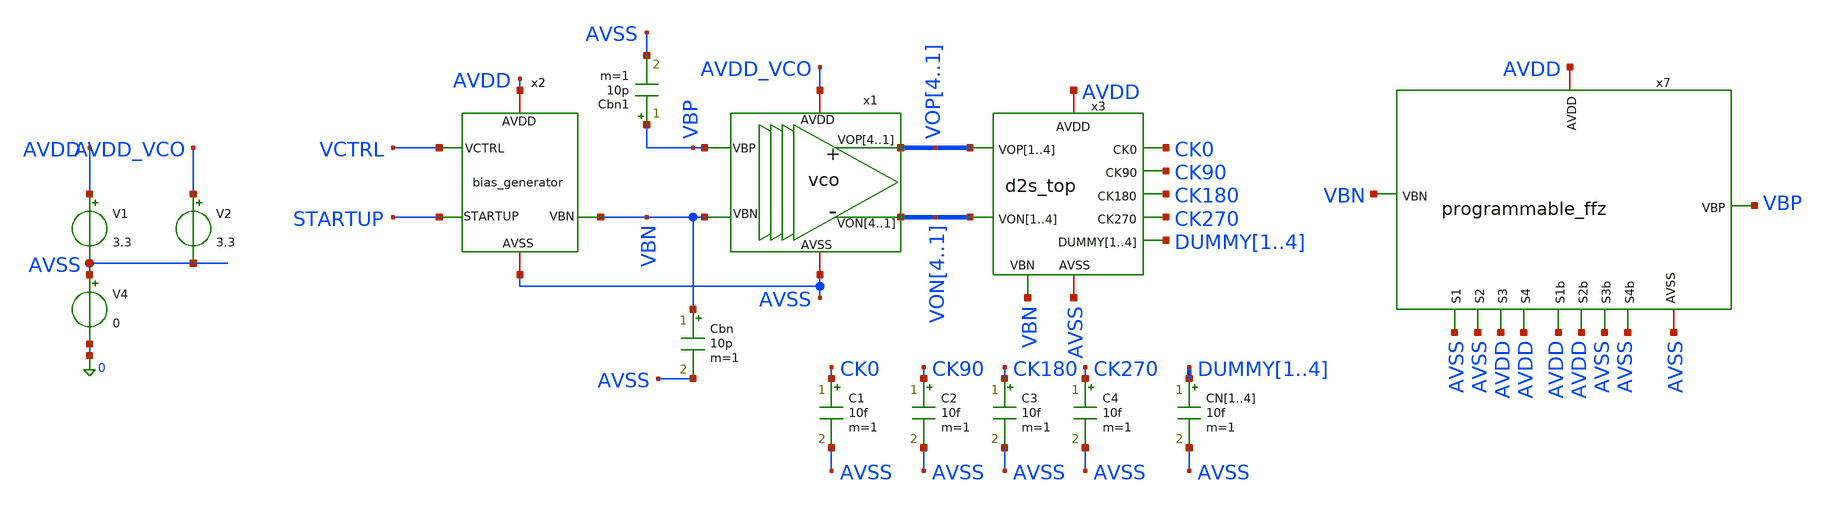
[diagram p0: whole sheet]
** sch_path: designs/libs/tb_analog/tb_quadrature_vco/tb_quadrature_vco.sch
**.subckt tb_quadrature_vco
x1 VOP4 VOP3 VOP2 VOP1 VON4 VON3 VON2 VON1 AVDD_VCO AVSS VBP VBN vco
V1 AVDD AVSS 3.3
V4 AVSS 0 0
CN1 DUMMY1 AVSS 10f m=1
CN2 DUMMY2 AVSS 10f m=1
CN3 DUMMY3 AVSS 10f m=1
CN4 DUMMY4 AVSS 10f m=1
x2 VCTRL AVDD STARTUP AVSS VBN bias_generator
Cbn VBN AVSS 10p m=1
V2 AVDD_VCO AVSS 3.3
Cbn1 VBP AVSS 10p m=1
x7 VBP AVSS AVDD VBN AVDD AVSS AVDD AVSS AVSS AVDD AVSS AVDD programmable_ffz
x3 VOP4 VOP3 VOP2 VOP1 VON4 VON3 VON2 VON1 VBN DUMMY1 DUMMY2 DUMMY3 DUMMY4 CK0 CK90 CK180 CK270 AVDD
+ AVSS d2s_top
C1 CK0 AVSS 10f m=1
C2 CK90 AVSS 10f m=1
C3 CK180 AVSS 10f m=1
C4 CK270 AVSS 10f m=1
**** begin user architecture code


.param Vin=0 Vcm=2.5
.ic v(vop1)=3.3 v(von1)=0 v(startup)=0 v(vbp)=0
.param t1=1u t2=2u t3=3u t4=4u t5=5u t6=6u t7=10u t8=50u t9=500u tr=10n

.param d0=0 d1=0.35 d2=0.825 d3=1.2375 d4=1.65 d5=2.0625 d6=2.475 d7=2.6 d8=2.75

*vs startup 0 pulse(0 1 100n 10n 10n 100n 100m)
*vctrl vctrl 0 pwl(0 d0
*+t1 d0 't1+tr' d1
*+t2 d1 't2+tr' d2
*+t3 d2 't3+tr' d3
*+t4 d3 't4+tr' d4
*+t5 d4 't5+tr' d5
*+t6 d5 't6+tr' d6
*+t7 d6 't7+tr' d7
*+t8 d7 't8+tr' d8
*+t9 d8 't9+tr' d0 R 0)

vctrl vctrl 0 d8

.control
set wr_singlescale
set wr_vecnames

save v(CK0) v(CK90) v(CK180) v(CK270) v(vctrl) v(vbp) v(vbn) v(dummy1) v(dummy2) v(dummy3) v(dummy4)
+ v(VOP1) v(VOP2) v(VOP3) v(VOP4) v(VON1) v(VON2) v(VON3) v(VON4)

OP
show all

*tran 1n 1.5m
tran 10n 500u
*tran 10p 50n



*let sum = v(VOP1) + v(VON1)
*let diff = v(VOP1) - v(VON1)
*let gain = deriv(diff)
*let vcm = AVG(sum/2)


*meas tran vmax MAX v(VOP1) FROM=10n TO=20n
*meas tran vmin MIN v(VOP1) FROM=10n TO=20n
*let vswing = vmax-vmin

meas tran I_tail_avg1 AVG i(v.x1.x1.vmeas) FROM=1.01u TO=2u
meas tran I_tail_avg2 AVG i(v.x1.x1.vmeas) FROM=2.01u TO=3u
meas tran I_tail_avg3 AVG i(v.x1.x1.vmeas) FROM=3.01u TO=4u
meas tran I_tail_avg4 AVG i(v.x1.x1.vmeas) FROM=4.01u TO=5u
meas tran I_tail_avg5 AVG i(v.x1.x1.vmeas) FROM=5.01u TO=6u
meas tran I_tail_avg6 AVG i(v.x1.x1.vmeas) FROM=6.01u TO=10u
meas tran I_tail_avg7 AVG i(v.x1.x1.vmeas) FROM=10.01u TO=50u
meas tran I_tail_avg8 AVG i(v.x1.x1.vmeas) FROM=50.01u TO=500u

*meas tran I_d2s1 AVG i(v.x3.x1.vmeas) FROM=1.01u TO=2u
*meas tran I_d2s2 AVG i(v.x3.x1.vmeas) FROM=2.01u TO=3u
*meas tran I_d2s3 AVG i(v.x3.x1.vmeas) FROM=3.01u TO=4u
*meas tran I_d2s4 AVG i(v.x3.x1.vmeas) FROM=4.01u TO=5u
*meas tran I_d2s5 AVG i(v.x3.x1.vmeas) FROM=5.01u TO=6u
*meas tran I_d2s6 AVG i(v.x3.x1.vmeas) FROM=6.01u TO=10u
*meas tran I_d2s7 AVG i(v.x3.x1.vmeas) FROM=10.01u TO=50u
*meas tran I_d2s8 AVG i(v.x3.x1.vmeas) FROM=50.01u TO=500u

*meas tran I_VCO1 AVG i(V2) FROM=1.01u TO=2u
*meas tran I_VCO2 AVG i(V2) FROM=2.01u TO=3u
*meas tran I_VCO3 AVG i(V2) FROM=3.01u TO=4u
*meas tran I_VCO4 AVG i(V2) FROM=4.01u TO=5u
*meas tran I_VCO5 AVG i(V2) FROM=5.01u TO=6u
*meas tran I_VCO6 AVG i(V2) FROM=6.01u TO=10u
*meas tran I_VCO7 AVG i(V2) FROM=10.01u TO=100u
*meas tran I_VCO8 AVG i(V2) FROM=100.01u TO=1m

remzerovec
*linearize v(CK0) v(CK90) v(CK180) v(CK270)
write tb_quadrature_vco.raw
destroy all
exit
*wrdata
*+ /foss/designs/synchronos-chipathon-2026/designs/libs/scripts/sim_data/tb_quadrature_vco_free_running_test.txt tran.all
.endc



.include $::180MCU_MODELS/design.ngspice
.lib $::180MCU_MODELS/sm141064.ngspice typical
*.lib $::180MCU_MODELS/sm141064.ngspice SS
*.lib $::180MCU_MODELS/sm141064.ngspice FF
*.lib $::180MCU_MODELS/sm141064.ngspice SF
*.lib $::180MCU_MODELS/sm141064.ngspice FS

**** end user architecture code
**.ends

* expanding   symbol:  libs/core_analog/vco/vco.sym # of pins=6
** sym_path: designs/libs/core_analog/vco/vco.sym
** sch_path: designs/libs/core_analog/vco/vco.sch
.subckt vco VOP4 VOP3 VOP2 VOP1 VON4 VON3 VON2 VON1 AVDD AVSS VBP VBN
*.opin VOP1,VOP2,VOP3,VOP4
*.opin VON1,VON2,VON3,VON4
*.ipin VBP
*.ipin VBN
*.iopin AVDD
*.iopin AVSS
x1 VOP1 AVDD VOP4 VON4 VON1 AVSS VBP VBN delay_stage
x2 VOP2 AVDD VON1 VOP1 VON2 AVSS VBP VBN delay_stage
x3 VOP3 AVDD VON2 VOP2 VON3 AVSS VBP VBN delay_stage
x4 VOP4 AVDD VON3 VOP3 VON4 AVSS VBP VBN delay_stage
.ends


* expanding   symbol:  libs/core_analog/bias_generator/bias_generator.sym # of pins=5
** sym_path: designs/libs/core_analog/bias_generator/bias_generator.sym
** sch_path: designs/libs/core_analog/bias_generator/bias_generator.sch
.subckt bias_generator VCTRL AVDD STARTUP AVSS VBN
*.ipin VCTRL
*.ipin STARTUP
*.iopin AVDD
*.iopin AVSS
*.opin VBN
x1 VBN AVDD net2 VCTRL AVSS net1 ota_5t
XM1 net1 net1 AVDD AVDD pfet_03v3 L=0.5u W=16.8u nf=1 ad='int((nf+1)/2) * W/nf * 0.18u' as='int((nf+2)/2) * W/nf * 0.18u'
+ pd='2*int((nf+1)/2) * (W/nf + 0.18u)' ps='2*int((nf+2)/2) * (W/nf + 0.18u)' nrd='0.18u / W' nrs='0.18u / W'
+ sa=0 sb=0 sd=0 m=16
XM8 net2 AVDD net4 AVSS nfet_03v3 L=0.5u W=2.08u nf=1 ad='int((nf+1)/2) * W/nf * 0.18u' as='int((nf+2)/2) * W/nf * 0.18u'
+ pd='2*int((nf+1)/2) * (W/nf + 0.18u)' ps='2*int((nf+2)/2) * (W/nf + 0.18u)' nrd='0.18u / W' nrs='0.18u / W'
+ sa=0 sb=0 sd=0 m=8
XM11 net1 AVDD net3 AVSS nfet_03v3 L=0.5u W=2.08u nf=1 ad='int((nf+1)/2) * W/nf * 0.18u' as='int((nf+2)/2) * W/nf * 0.18u'
+ pd='2*int((nf+1)/2) * (W/nf + 0.18u)' ps='2*int((nf+2)/2) * (W/nf + 0.18u)' nrd='0.18u / W' nrs='0.18u / W'
+ sa=0 sb=0 sd=0 m=8
XM2 net2 VCTRL AVDD AVDD pfet_03v3 L=1.5u W=1.1u nf=1 ad='int((nf+1)/2) * W/nf * 0.18u' as='int((nf+2)/2) * W/nf * 0.18u'
+ pd='2*int((nf+1)/2) * (W/nf + 0.18u)' ps='2*int((nf+2)/2) * (W/nf + 0.18u)' nrd='0.18u / W' nrs='0.18u / W'
+ sa=0 sb=0 sd=0 m=8
XM5 net2 net2 AVDD AVDD pfet_03v3 L=1.5u W=1.1u nf=1 ad='int((nf+1)/2) * W/nf * 0.18u' as='int((nf+2)/2) * W/nf * 0.18u'
+ pd='2*int((nf+1)/2) * (W/nf + 0.18u)' ps='2*int((nf+2)/2) * (W/nf + 0.18u)' nrd='0.18u / W' nrs='0.18u / W'
+ sa=0 sb=0 sd=0 m=8
XM7 net4 VBN AVSS AVSS nfet_03v3 L=0.5u W=11.25u nf=1 ad='int((nf+1)/2) * W/nf * 0.18u' as='int((nf+2)/2) * W/nf * 0.18u'
+ pd='2*int((nf+1)/2) * (W/nf + 0.18u)' ps='2*int((nf+2)/2) * (W/nf + 0.18u)' nrd='0.18u / W' nrs='0.18u / W'
+ sa=0 sb=0 sd=0 m=8
XM3 net3 VBN AVSS AVSS nfet_03v3 L=0.5u W=11.25u nf=1 ad='int((nf+1)/2) * W/nf * 0.18u' as='int((nf+2)/2) * W/nf * 0.18u'
+ pd='2*int((nf+1)/2) * (W/nf + 0.18u)' ps='2*int((nf+2)/2) * (W/nf + 0.18u)' nrd='0.18u / W' nrs='0.18u / W'
+ sa=0 sb=0 sd=0 m=8
XM4 net3 STARTUP AVSS AVSS nfet_03v3 L=0.5u W=11.25u nf=1 ad='int((nf+1)/2) * W/nf * 0.18u' as='int((nf+2)/2) * W/nf * 0.18u'
+ pd='2*int((nf+1)/2) * (W/nf + 0.18u)' ps='2*int((nf+2)/2) * (W/nf + 0.18u)' nrd='0.18u / W' nrs='0.18u / W'
+ sa=0 sb=0 sd=0 m=2
.ends


* expanding   symbol:  libs/core_analog/programmable_ffz/programmable_ffz.sym # of pins=12
** sym_path: designs/libs/core_analog/programmable_ffz/programmable_ffz.sym
** sch_path: designs/libs/core_analog/programmable_ffz/programmable_ffz.sch
.subckt programmable_ffz VBP AVSS AVDD VBN S1b S1 S2b S2 S3b S3 S4b S4
*.ipin VBN
*.ipin S1b
*.ipin S1
*.ipin S2b
*.ipin S2
*.ipin S3b
*.ipin S3
*.ipin S4b
*.ipin S4
*.iopin AVSS
*.iopin AVDD
*.opin VBP
x2 VBN AVSS S1 VBN1 S1b AVDD transmission_gate
x3 VBN AVSS S2 VBN2 S2b AVDD transmission_gate
x4 VBN AVSS S3 VBN3 S3b AVDD transmission_gate
x5 VBN AVSS S4 VBN4 S4b AVDD transmission_gate
x1 AVDD VBP VBN AVSS AVSS feed_forward_zero
x6 AVDD net1 VBN1 S1b AVSS feed_forward_zero
x71 AVDD net2[1] VBN2 S2b AVSS feed_forward_zero
x72 AVDD net2[0] VBN2 S2b AVSS feed_forward_zero
x11 AVDD net3[3] VBN3 S3b AVSS feed_forward_zero
x12 AVDD net3[2] VBN3 S3b AVSS feed_forward_zero
x13 AVDD net3[1] VBN3 S3b AVSS feed_forward_zero
x14 AVDD net3[0] VBN3 S3b AVSS feed_forward_zero
x21 AVDD net4[7] VBN4 S4b AVSS feed_forward_zero
x22 AVDD net4[6] VBN4 S4b AVSS feed_forward_zero
x23 AVDD net4[5] VBN4 S4b AVSS feed_forward_zero
x24 AVDD net4[4] VBN4 S4b AVSS feed_forward_zero
x25 AVDD net4[3] VBN4 S4b AVSS feed_forward_zero
x26 AVDD net4[2] VBN4 S4b AVSS feed_forward_zero
x27 AVDD net4[1] VBN4 S4b AVSS feed_forward_zero
x28 AVDD net4[0] VBN4 S4b AVSS feed_forward_zero
x7 net1 AVSS S1 VBP S1b AVDD transmission_gate
x81 net2[1] AVSS S2 VBP S2b AVDD transmission_gate
x82 net2[0] AVSS S2 VBP S2b AVDD transmission_gate
x91 net3[3] AVSS S3 VBP S3b AVDD transmission_gate
x92 net3[2] AVSS S3 VBP S3b AVDD transmission_gate
x93 net3[1] AVSS S3 VBP S3b AVDD transmission_gate
x94 net3[0] AVSS S3 VBP S3b AVDD transmission_gate
x101 net4[7] AVSS S4 VBP S4b AVDD transmission_gate
x102 net4[6] AVSS S4 VBP S4b AVDD transmission_gate
x103 net4[5] AVSS S4 VBP S4b AVDD transmission_gate
x104 net4[4] AVSS S4 VBP S4b AVDD transmission_gate
x105 net4[3] AVSS S4 VBP S4b AVDD transmission_gate
x106 net4[2] AVSS S4 VBP S4b AVDD transmission_gate
x107 net4[1] AVSS S4 VBP S4b AVDD transmission_gate
x108 net4[0] AVSS S4 VBP S4b AVDD transmission_gate
.ends


* expanding   symbol:  libs/core_analog/d2s_top/d2s_top.sym # of pins=10
** sym_path: designs/libs/core_analog/d2s_top/d2s_top.sym
** sch_path: designs/libs/core_analog/d2s_top/d2s_top.sch
.subckt d2s_top VOP1 VOP2 VOP3 VOP4 VON1 VON2 VON3 VON4 VBN DUMMY1 DUMMY2 DUMMY3 DUMMY4 CK0 CK90
+ CK180 CK270 AVDD AVSS
*.ipin VOP1,VOP2,VOP3,VOP4
*.ipin VON1,VON2,VON3,VON4
*.ipin VBN
*.opin DUMMY1,DUMMY2,DUMMY3,DUMMY4
*.opin CK0
*.opin CK90
*.opin CK180
*.opin CK270
*.iopin AVDD
*.iopin AVSS
x1 AVDD AVSS VON1 VOP1 VBN net8 d2s_converter
x2 AVDD AVSS VON3 VOP3 VBN net1 d2s_converter
x9 AVDD net8 CK0 AVSS inv
x10 AVDD net1 CK90 AVSS inv
x3 AVDD AVSS VOP1 VON1 VBN net2 d2s_converter
x4 AVDD net2 CK180 AVSS inv
x5 AVDD AVSS VOP3 VON3 VBN net3 d2s_converter
x6 AVDD net3 CK270 AVSS inv
x7 AVDD AVSS VON2 VOP2 VBN net7 d2s_converter
x8 AVDD AVSS VON4 VOP4 VBN net4 d2s_converter
x11 AVDD net7 DUMMY1 AVSS inv
x12 AVDD net4 DUMMY2 AVSS inv
x13 AVDD AVSS VOP2 VON2 VBN net5 d2s_converter
x14 AVDD net5 DUMMY3 AVSS inv
x15 AVDD AVSS VOP4 VON4 VBN net6 d2s_converter
x16 AVDD net6 DUMMY4 AVSS inv
.ends


* expanding   symbol:  libs/core_analog/delay_stage/delay_stage.sym # of pins=8
** sym_path: designs/libs/core_analog/delay_stage/delay_stage.sym
** sch_path: designs/libs/core_analog/delay_stage/delay_stage.sch
.subckt delay_stage VOP AVDD VIP VIN VON AVSS VBP VBN
*.ipin VIP
*.ipin VIN
*.opin VOP
*.opin VON
*.iopin AVDD
*.iopin AVSS
*.ipin VBP
*.ipin VBN
XM5 VON VIP net1 AVSS nfet_03v3 L=0.5u W=2.08u nf=1 ad='int((nf+1)/2) * W/nf * 0.18u' as='int((nf+2)/2) * W/nf * 0.18u'
+ pd='2*int((nf+1)/2) * (W/nf + 0.18u)' ps='2*int((nf+2)/2) * (W/nf + 0.18u)' nrd='0.18u / W' nrs='0.18u / W'
+ sa=0 sb=0 sd=0 m=8
XM2 VON VON AVDD AVDD pfet_03v3 L=1.5u W=1.1u nf=1 ad='int((nf+1)/2) * W/nf * 0.18u' as='int((nf+2)/2) * W/nf * 0.18u'
+ pd='2*int((nf+1)/2) * (W/nf + 0.18u)' ps='2*int((nf+2)/2) * (W/nf + 0.18u)' nrd='0.18u / W' nrs='0.18u / W'
+ sa=0 sb=0 sd=0 m=8
XM6 VOP VIN net1 AVSS nfet_03v3 L=0.5u W=2.08u nf=1 ad='int((nf+1)/2) * W/nf * 0.18u' as='int((nf+2)/2) * W/nf * 0.18u'
+ pd='2*int((nf+1)/2) * (W/nf + 0.18u)' ps='2*int((nf+2)/2) * (W/nf + 0.18u)' nrd='0.18u / W' nrs='0.18u / W'
+ sa=0 sb=0 sd=0 m=8
XM1 VON VBP AVDD AVDD pfet_03v3 L=1.5u W=1.1u nf=1 ad='int((nf+1)/2) * W/nf * 0.18u' as='int((nf+2)/2) * W/nf * 0.18u'
+ pd='2*int((nf+1)/2) * (W/nf + 0.18u)' ps='2*int((nf+2)/2) * (W/nf + 0.18u)' nrd='0.18u / W' nrs='0.18u / W'
+ sa=0 sb=0 sd=0 m=8
XM3 VOP VBP AVDD AVDD pfet_03v3 L=1.5u W=1.1u nf=1 ad='int((nf+1)/2) * W/nf * 0.18u' as='int((nf+2)/2) * W/nf * 0.18u'
+ pd='2*int((nf+1)/2) * (W/nf + 0.18u)' ps='2*int((nf+2)/2) * (W/nf + 0.18u)' nrd='0.18u / W' nrs='0.18u / W'
+ sa=0 sb=0 sd=0 m=8
XM4 VOP VOP AVDD AVDD pfet_03v3 L=1.5u W=1.1u nf=1 ad='int((nf+1)/2) * W/nf * 0.18u' as='int((nf+2)/2) * W/nf * 0.18u'
+ pd='2*int((nf+1)/2) * (W/nf + 0.18u)' ps='2*int((nf+2)/2) * (W/nf + 0.18u)' nrd='0.18u / W' nrs='0.18u / W'
+ sa=0 sb=0 sd=0 m=8
XM8 net1 VBN AVSS AVSS nfet_03v3 L=0.5u W=11.25u nf=1 ad='int((nf+1)/2) * W/nf * 0.18u' as='int((nf+2)/2) * W/nf * 0.18u'
+ pd='2*int((nf+1)/2) * (W/nf + 0.18u)' ps='2*int((nf+2)/2) * (W/nf + 0.18u)' nrd='0.18u / W' nrs='0.18u / W'
+ sa=0 sb=0 sd=0 m=8
.ends


* expanding   symbol:  libs/core_analog/ota_5t/ota_5t.sym # of pins=6
** sym_path: designs/libs/core_analog/ota_5t/ota_5t.sym
** sch_path: designs/libs/core_analog/ota_5t/ota_5t.sch
.subckt ota_5t VO AVDD VI+ VI- AVSS VB
*.ipin VI+
*.ipin VI-
*.ipin VB
*.iopin AVDD
*.iopin AVSS
*.opin VO
XM1 VO VI- net2 AVDD pfet_03v3 L=0.5u W=6.55u nf=1 ad='int((nf+1)/2) * W/nf * 0.18u' as='int((nf+2)/2) * W/nf * 0.18u'
+ pd='2*int((nf+1)/2) * (W/nf + 0.18u)' ps='2*int((nf+2)/2) * (W/nf + 0.18u)' nrd='0.18u / W' nrs='0.18u / W'
+ sa=0 sb=0 sd=0 m=8
XM4 VO net1 AVSS AVSS nfet_03v3 L=0.5u W=4.8u nf=1 ad='int((nf+1)/2) * W/nf * 0.18u' as='int((nf+2)/2) * W/nf * 0.18u'
+ pd='2*int((nf+1)/2) * (W/nf + 0.18u)' ps='2*int((nf+2)/2) * (W/nf + 0.18u)' nrd='0.18u / W' nrs='0.18u / W'
+ sa=0 sb=0 sd=0 m=4
XM3 net2 VB net3 AVDD pfet_03v3 L=0.5u W=8.3u nf=1 ad='int((nf+1)/2) * W/nf * 0.18u' as='int((nf+2)/2) * W/nf * 0.18u'
+ pd='2*int((nf+1)/2) * (W/nf + 0.18u)' ps='2*int((nf+2)/2) * (W/nf + 0.18u)' nrd='0.18u / W' nrs='0.18u / W'
+ sa=0 sb=0 sd=0 m=16
XM2 net1 VI+ net2 AVDD pfet_03v3 L=0.5u W=6.55u nf=1 ad='int((nf+1)/2) * W/nf * 0.18u' as='int((nf+2)/2) * W/nf * 0.18u'
+ pd='2*int((nf+1)/2) * (W/nf + 0.18u)' ps='2*int((nf+2)/2) * (W/nf + 0.18u)' nrd='0.18u / W' nrs='0.18u / W'
+ sa=0 sb=0 sd=0 m=8
XM5 net1 net1 AVSS AVSS nfet_03v3 L=0.5u W=4.8u nf=1 ad='int((nf+1)/2) * W/nf * 0.18u' as='int((nf+2)/2) * W/nf * 0.18u'
+ pd='2*int((nf+1)/2) * (W/nf + 0.18u)' ps='2*int((nf+2)/2) * (W/nf + 0.18u)' nrd='0.18u / W' nrs='0.18u / W'
+ sa=0 sb=0 sd=0 m=4
Vmeas AVDD net3 0
.save i(vmeas)
.ends


* expanding   symbol:  libs/core_analog/transmission_gate/transmission_gate.sym # of pins=6
** sym_path: designs/libs/core_analog/transmission_gate/transmission_gate.sym
** sch_path: designs/libs/core_analog/transmission_gate/transmission_gate.sch
.subckt transmission_gate ind vss clkn ins clkp vdd
*.iopin ind
*.iopin ins
*.iopin clkn
*.iopin clkp
*.iopin vdd
*.iopin vss
XM1 ind clkp ins vdd pfet_03v3 L=0.5u W=3.0u nf=1 ad='int((nf+1)/2) * W/nf * 0.18u' as='int((nf+2)/2) * W/nf * 0.18u'
+ pd='2*int((nf+1)/2) * (W/nf + 0.18u)' ps='2*int((nf+2)/2) * (W/nf + 0.18u)' nrd='0.18u / W' nrs='0.18u / W'
+ sa=0 sb=0 sd=0 m=1
XM2 ind clkn ins vss nfet_03v3 L=0.5u W=1.0u nf=1 ad='int((nf+1)/2) * W/nf * 0.18u' as='int((nf+2)/2) * W/nf * 0.18u'
+ pd='2*int((nf+1)/2) * (W/nf + 0.18u)' ps='2*int((nf+2)/2) * (W/nf + 0.18u)' nrd='0.18u / W' nrs='0.18u / W'
+ sa=0 sb=0 sd=0 m=1
.ends


* expanding   symbol:  libs/core_analog/feed_forward_zero/feed_forward_zero.sym # of pins=5
** sym_path: designs/libs/core_analog/feed_forward_zero/feed_forward_zero.sym
** sch_path: designs/libs/core_analog/feed_forward_zero/feed_forward_zero.sch
.subckt feed_forward_zero AVDD VBP VBN S AVSS
*.opin VBP
*.iopin AVDD
*.iopin AVSS
*.ipin VBN
*.ipin S
XM1 VBP VBP AVDD AVDD pfet_03v3 L=1.5u W=1.1u nf=1 ad='int((nf+1)/2) * W/nf * 0.18u' as='int((nf+2)/2) * W/nf * 0.18u'
+ pd='2*int((nf+1)/2) * (W/nf + 0.18u)' ps='2*int((nf+2)/2) * (W/nf + 0.18u)' nrd='0.18u / W' nrs='0.18u / W'
+ sa=0 sb=0 sd=0 m=2
XM2 VBP VBP AVDD AVDD pfet_03v3 L=1.5u W=1.1u nf=1 ad='int((nf+1)/2) * W/nf * 0.18u' as='int((nf+2)/2) * W/nf * 0.18u'
+ pd='2*int((nf+1)/2) * (W/nf + 0.18u)' ps='2*int((nf+2)/2) * (W/nf + 0.18u)' nrd='0.18u / W' nrs='0.18u / W'
+ sa=0 sb=0 sd=0 m=2
XM3 VBP AVDD net1 AVSS nfet_03v3 L=0.5u W=2.08u nf=1 ad='int((nf+1)/2) * W/nf * 0.18u' as='int((nf+2)/2) * W/nf * 0.18u'
+ pd='2*int((nf+1)/2) * (W/nf + 0.18u)' ps='2*int((nf+2)/2) * (W/nf + 0.18u)' nrd='0.18u / W' nrs='0.18u / W'
+ sa=0 sb=0 sd=0 m=2
XM4 net1 VBN AVSS AVSS nfet_03v3 L=0.5u W=11.25u nf=1 ad='int((nf+1)/2) * W/nf * 0.18u' as='int((nf+2)/2) * W/nf * 0.18u'
+ pd='2*int((nf+1)/2) * (W/nf + 0.18u)' ps='2*int((nf+2)/2) * (W/nf + 0.18u)' nrd='0.18u / W' nrs='0.18u / W'
+ sa=0 sb=0 sd=0 m=2
XM7 VBN S AVSS AVSS nfet_03v3 L=0.5u W=1u nf=1 ad='int((nf+1)/2) * W/nf * 0.18u' as='int((nf+2)/2) * W/nf * 0.18u'
+ pd='2*int((nf+1)/2) * (W/nf + 0.18u)' ps='2*int((nf+2)/2) * (W/nf + 0.18u)' nrd='0.18u / W' nrs='0.18u / W'
+ sa=0 sb=0 sd=0 m=1
.ends


* expanding   symbol:  libs/core_analog/d2s_converter/d2s_converter.sym # of pins=6
** sym_path: designs/libs/core_analog/d2s_converter/d2s_converter.sym
** sch_path: designs/libs/core_analog/d2s_converter/d2s_converter.sch
.subckt d2s_converter AVDD AVSS VIN VIP VBN VO
*.iopin AVDD
*.iopin AVSS
*.ipin VIN
*.ipin VIP
*.opin VO
*.ipin VBN
XM2 VOPB VIN i1 AVSS nfet_03v3 L=0.3u W=1.9u nf=1 ad='int((nf+1)/2) * W/nf * 0.18u' as='int((nf+2)/2) * W/nf * 0.18u'
+ pd='2*int((nf+1)/2) * (W/nf + 0.18u)' ps='2*int((nf+2)/2) * (W/nf + 0.18u)' nrd='0.18u / W' nrs='0.18u / W'
+ sa=0 sb=0 sd=0 m=4
XM4 VOPB VOPB AVDD AVDD pfet_03v3 L=0.3u W=1.4u nf=1 ad='int((nf+1)/2) * W/nf * 0.18u' as='int((nf+2)/2) * W/nf * 0.18u'
+ pd='2*int((nf+1)/2) * (W/nf + 0.18u)' ps='2*int((nf+2)/2) * (W/nf + 0.18u)' nrd='0.18u / W' nrs='0.18u / W'
+ sa=0 sb=0 sd=0 m=4
XM11 VOB VOB AVSS AVSS nfet_03v3 L=0.3u W=1.5u nf=1 ad='int((nf+1)/2) * W/nf * 0.18u' as='int((nf+2)/2) * W/nf * 0.18u'
+ pd='2*int((nf+1)/2) * (W/nf + 0.18u)' ps='2*int((nf+2)/2) * (W/nf + 0.18u)' nrd='0.18u / W' nrs='0.18u / W'
+ sa=0 sb=0 sd=0 m=4
XM13 VOB VOP AVDD AVDD pfet_03v3 L=0.3u W=2u nf=1 ad='int((nf+1)/2) * W/nf * 0.18u' as='int((nf+2)/2) * W/nf * 0.18u'
+ pd='2*int((nf+1)/2) * (W/nf + 0.18u)' ps='2*int((nf+2)/2) * (W/nf + 0.18u)' nrd='0.18u / W' nrs='0.18u / W'
+ sa=0 sb=0 sd=0 m=4
XM3 VOP VIP i1 AVSS nfet_03v3 L=0.3u W=1.9u nf=1 ad='int((nf+1)/2) * W/nf * 0.18u' as='int((nf+2)/2) * W/nf * 0.18u'
+ pd='2*int((nf+1)/2) * (W/nf + 0.18u)' ps='2*int((nf+2)/2) * (W/nf + 0.18u)' nrd='0.18u / W' nrs='0.18u / W'
+ sa=0 sb=0 sd=0 m=4
XM5 VOP VOPB AVDD AVDD pfet_03v3 L=0.3u W=1.4u nf=1 ad='int((nf+1)/2) * W/nf * 0.18u' as='int((nf+2)/2) * W/nf * 0.18u'
+ pd='2*int((nf+1)/2) * (W/nf + 0.18u)' ps='2*int((nf+2)/2) * (W/nf + 0.18u)' nrd='0.18u / W' nrs='0.18u / W'
+ sa=0 sb=0 sd=0 m=4
XM7 VONB VIP i2 AVSS nfet_03v3 L=0.3u W=1.9u nf=1 ad='int((nf+1)/2) * W/nf * 0.18u' as='int((nf+2)/2) * W/nf * 0.18u'
+ pd='2*int((nf+1)/2) * (W/nf + 0.18u)' ps='2*int((nf+2)/2) * (W/nf + 0.18u)' nrd='0.18u / W' nrs='0.18u / W'
+ sa=0 sb=0 sd=0 m=4
XM8 VONB VONB AVDD AVDD pfet_03v3 L=0.3u W=1.4u nf=1 ad='int((nf+1)/2) * W/nf * 0.18u' as='int((nf+2)/2) * W/nf * 0.18u'
+ pd='2*int((nf+1)/2) * (W/nf + 0.18u)' ps='2*int((nf+2)/2) * (W/nf + 0.18u)' nrd='0.18u / W' nrs='0.18u / W'
+ sa=0 sb=0 sd=0 m=4
XM9 VON VIN i2 AVSS nfet_03v3 L=0.3u W=1.9u nf=1 ad='int((nf+1)/2) * W/nf * 0.18u' as='int((nf+2)/2) * W/nf * 0.18u'
+ pd='2*int((nf+1)/2) * (W/nf + 0.18u)' ps='2*int((nf+2)/2) * (W/nf + 0.18u)' nrd='0.18u / W' nrs='0.18u / W'
+ sa=0 sb=0 sd=0 m=4
XM10 VON VONB AVDD AVDD pfet_03v3 L=0.3u W=1.4u nf=1 ad='int((nf+1)/2) * W/nf * 0.18u' as='int((nf+2)/2) * W/nf * 0.18u'
+ pd='2*int((nf+1)/2) * (W/nf + 0.18u)' ps='2*int((nf+2)/2) * (W/nf + 0.18u)' nrd='0.18u / W' nrs='0.18u / W'
+ sa=0 sb=0 sd=0 m=4
XM14 VO VON AVDD AVDD pfet_03v3 L=0.3u W=2u nf=1 ad='int((nf+1)/2) * W/nf * 0.18u' as='int((nf+2)/2) * W/nf * 0.18u'
+ pd='2*int((nf+1)/2) * (W/nf + 0.18u)' ps='2*int((nf+2)/2) * (W/nf + 0.18u)' nrd='0.18u / W' nrs='0.18u / W'
+ sa=0 sb=0 sd=0 m=4
XM12 VO VOB AVSS AVSS nfet_03v3 L=0.3u W=1.5u nf=1 ad='int((nf+1)/2) * W/nf * 0.18u' as='int((nf+2)/2) * W/nf * 0.18u'
+ pd='2*int((nf+1)/2) * (W/nf + 0.18u)' ps='2*int((nf+2)/2) * (W/nf + 0.18u)' nrd='0.18u / W' nrs='0.18u / W'
+ sa=0 sb=0 sd=0 m=4
XM1 i1 VBN AVSS AVSS nfet_03v3 L=0.5u W=11.25u nf=1 ad='int((nf+1)/2) * W/nf * 0.18u' as='int((nf+2)/2) * W/nf * 0.18u'
+ pd='2*int((nf+1)/2) * (W/nf + 0.18u)' ps='2*int((nf+2)/2) * (W/nf + 0.18u)' nrd='0.18u / W' nrs='0.18u / W'
+ sa=0 sb=0 sd=0 m=4
XM6 i2 VBN AVSS AVSS nfet_03v3 L=0.5u W=11.25u nf=1 ad='int((nf+1)/2) * W/nf * 0.18u' as='int((nf+2)/2) * W/nf * 0.18u'
+ pd='2*int((nf+1)/2) * (W/nf + 0.18u)' ps='2*int((nf+2)/2) * (W/nf + 0.18u)' nrd='0.18u / W' nrs='0.18u / W'
+ sa=0 sb=0 sd=0 m=4
.ends


* expanding   symbol:  libs/core_analog/inv/inv.sym # of pins=4
** sym_path: designs/libs/core_analog/inv/inv.sym
** sch_path: designs/libs/core_analog/inv/inv.sch
.subckt inv AVDD IN OUT AVSS
*.ipin IN
*.iopin AVDD
*.iopin AVSS
*.opin OUT
XM1 OUT IN AVDD AVDD pfet_03v3 L=0.28u W=0.9u nf=1 ad='int((nf+1)/2) * W/nf * 0.18u' as='int((nf+2)/2) * W/nf * 0.18u'
+ pd='2*int((nf+1)/2) * (W/nf + 0.18u)' ps='2*int((nf+2)/2) * (W/nf + 0.18u)' nrd='0.18u / W' nrs='0.18u / W'
+ sa=0 sb=0 sd=0 m=1
XM2 OUT IN AVSS AVSS nfet_03v3 L=0.28u W=0.3u nf=1 ad='int((nf+1)/2) * W/nf * 0.18u' as='int((nf+2)/2) * W/nf * 0.18u'
+ pd='2*int((nf+1)/2) * (W/nf + 0.18u)' ps='2*int((nf+2)/2) * (W/nf + 0.18u)' nrd='0.18u / W' nrs='0.18u / W'
+ sa=0 sb=0 sd=0 m=1
.ends

.end
